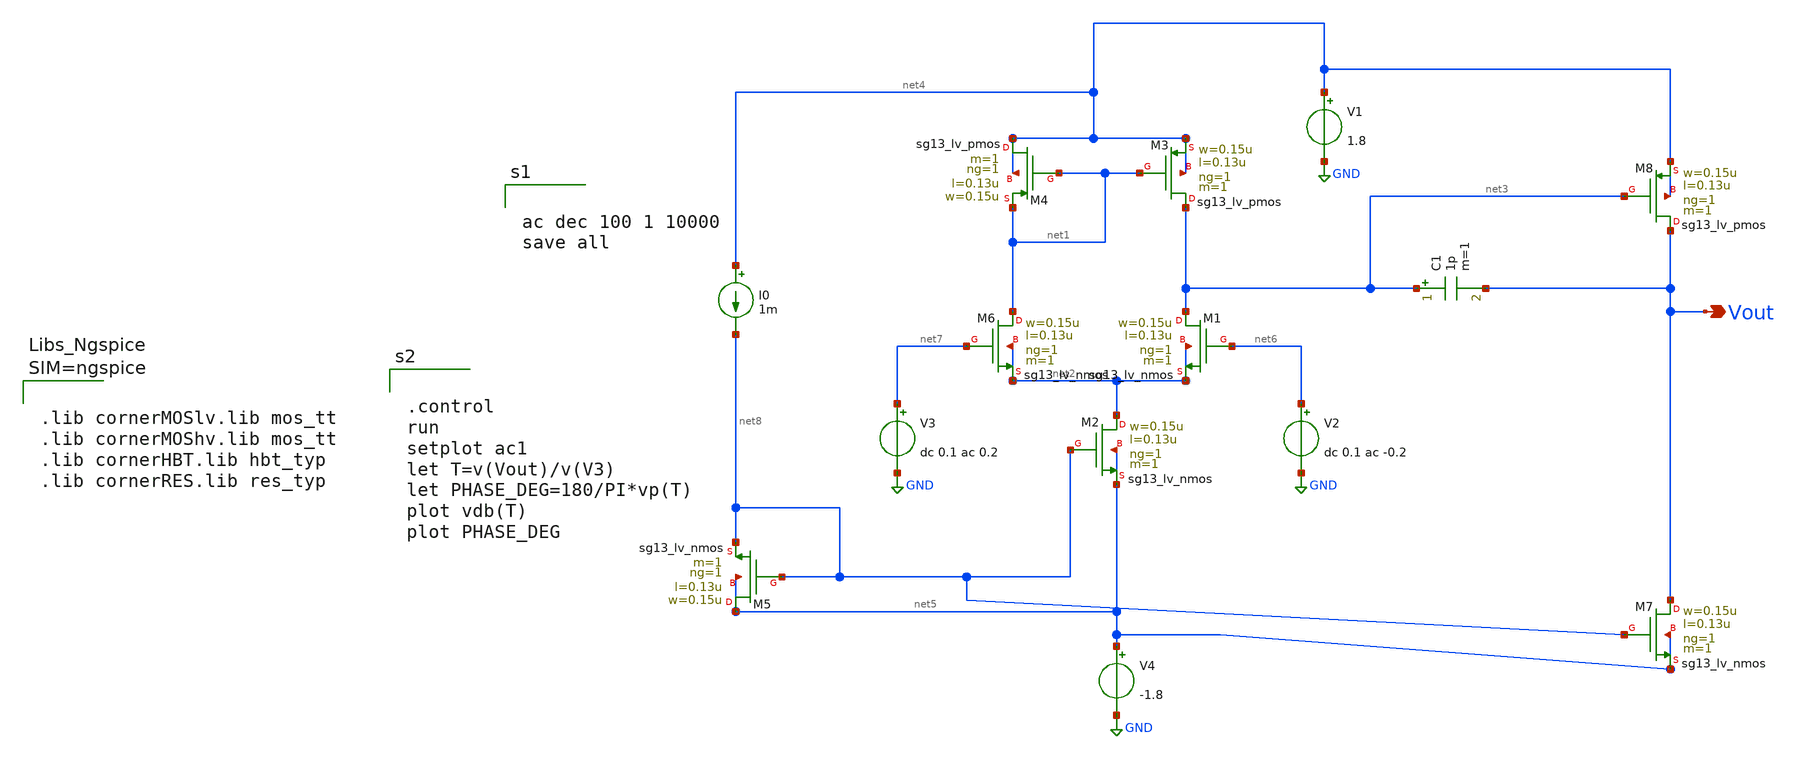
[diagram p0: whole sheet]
** sch_path: twostage.sch
**.subckt twostage Vout
*.opin Vout
V1 net4 GND 1.8
XM6 net1 net7 net2 net2 sg13_lv_nmos w=0.15u l=0.13u ng=1 m=1 mm_ok=1
XM1 net3 net6 net2 net2 sg13_lv_nmos w=0.15u l=0.13u ng=1 m=1 mm_ok=1
XM2 net2 net8 net5 net5 sg13_lv_nmos w=0.15u l=0.13u ng=1 m=1 mm_ok=1
XM3 net3 net1 net4 net4 sg13_lv_pmos w=0.15u l=0.13u ng=1 m=1 mm_ok=1
XM4 net4 net1 net1 net4 sg13_lv_pmos w=0.15u l=0.13u ng=1 m=1 mm_ok=1
V2 net6 GND dc 0.1 ac -0.2
V3 net7 GND dc 0.1 ac 0.2
V4 net5 GND -1.8
I0 net4 net8 1m
XM5 net5 net8 net8 net5 sg13_lv_nmos w=0.15u l=0.13u ng=1 m=1 mm_ok=1
XM7 Vout net8 net5 net5 sg13_lv_nmos w=0.15u l=0.13u ng=1 m=1 mm_ok=1
XM8 Vout net3 net4 net4 sg13_lv_pmos w=0.15u l=0.13u ng=1 m=1 mm_ok=1
C1 net3 Vout 1p m=1
**** begin user architecture code


ac dec 100 1 10000
save all




.control
run
setplot ac1
let T=v(Vout)/v(V3)
let PHASE_DEG=180/PI*vp(T)
plot vdb(T)
plot PHASE_DEG





.lib cornerMOSlv.lib mos_tt
.lib cornerMOShv.lib mos_tt
.lib cornerHBT.lib hbt_typ
.lib cornerRES.lib res_typ



**** end user architecture code
**.ends
.GLOBAL GND
.end
